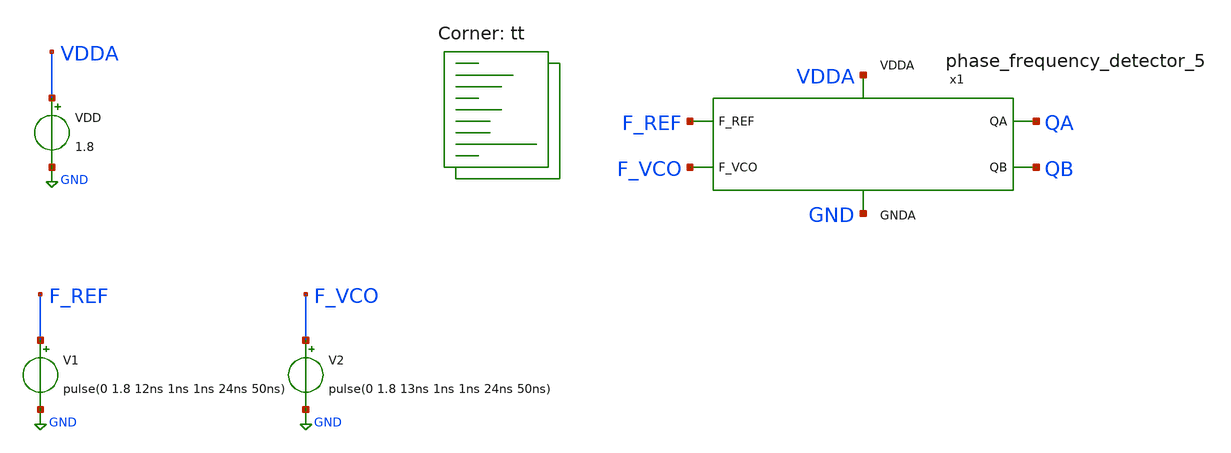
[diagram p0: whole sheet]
** sch_path: projects/pll/pfd/xschem_ngspice/tb_phase_frequency_detector.sch
**.subckt tb_phase_frequency_detector
V1 F_REF GND pulse(0 1.8 12ns 1ns 1ns 24ns 50ns)
V2 F_VCO GND pulse(0 1.8 13ns 1ns 1ns 24ns 50ns)
VDD VDDA GND 1.8
x1 F_REF F_VCO VDDA QA QB GND phase_frequency_detector_5
**** begin user architecture code
.lib $::SKYWATER_MODELS/sky130.lib.spice tt



.include /foss/pdks/sky130A/libs.ref/sky130_fd_sc_hd/spice/sky130_fd_sc_hd.spice


.option wnflag=1
.option method=gear trtol=1

* .ic v(osc)=0
* .temp = 75

.save v(x1.reset)
.save v(x1.qb_b)
.save v(x1.qa_b)
.save v(x1.f_b)
.save v(x1.f)
.save v(x1.e_b)
.save v(x1.e)
.save v(x1.before_reset)
.save v(qb)
.save v(qa)
.save v(f_vco)
.save v(f_ref)
.save v(f_vco)


.control

  tran 1ns 1us
  remzerovec
  * write tb_phase_frequency_detector.raw
  write tb_phase_frequency_detector_2.raw
  * linearize v(qa) v(qb)
  * wrdata
+ /foss/designs/my_design/projects/pll/pfd/xschem_ngspice/tb_phase_frequency_detector_QA.txt v(qa)
  * wrdata
+ /foss/designs/my_design/projects/pll/pfd/xschem_ngspice/tb_phase_frequency_detector_QB.txt v(qb)

  set appendwrite

.endc






**** end user architecture code
**.ends

* expanding   symbol:
*+  /foss/designs/my_design/projects/pll/pfd/xschem_ngspice/phase_frequency_detector_5.sym # of pins=6
** sym_path: projects/pll/pfd/xschem_ngspice/phase_frequency_detector_5.sym
** sch_path: projects/pll/pfd/xschem_ngspice/phase_frequency_detector_5.sch
.subckt phase_frequency_detector_5 F_REF F_VCO VDDA QA QB GNDA
*.ipin F_REF
*.opin QA
*.ipin F_VCO
*.opin QB
*.ipin VDDA
*.ipin GNDA
x1 VDDA GNDA QA F_REF QA_b nor_pfd
x2 VDDA GNDA QB F_VCO QB_b nor_pfd
x3 VDDA GNDA QA_b E QA nor_pfd
x4 VDDA GNDA QB_b F QB nor_pfd
x5 VDDA GNDA E_b QA_b E nor_pfd
x6 VDDA GNDA F_b QB_b F nor_pfd
x7 VDDA GNDA E Reset E_b nor_pfd
x12 VDDA GNDA F Reset F_b nor_pfd
x8 VDDA GNDA QB QA before_Reset nand_pfd
x9 VDDA GNDA before_Reset net1 inv_pfd
x10 VDDA GNDA net1 net2 inv_pfd
x11 VDDA GNDA net2 net3 inv_pfd
x13 VDDA GNDA net3 net4 inv_pfd
x14 VDDA GNDA net4 Reset inv_pfd
.ends


* expanding   symbol:  /foss/designs/my_design/projects/pll/pfd/xschem_ngspice/nor_pfd.sym # of
*+ pins=5
** sym_path: projects/pll/pfd/xschem_ngspice/nor_pfd.sym
** sch_path: projects/pll/pfd/xschem_ngspice/nor_pfd.sch
.subckt nor_pfd VDDA GNDA A B Y
*.ipin A
*.opin Y
*.ipin VDDA
*.ipin GNDA
*.ipin B
XM4 net1 B VDDA VDDA sky130_fd_pr__pfet_01v8 L=0.15 W=2 nf=1 ad='int((nf+1)/2) * W/nf * 0.29' as='int((nf+2)/2) * W/nf * 0.29'
+ pd='2*int((nf+1)/2) * (W/nf + 0.29)' ps='2*int((nf+2)/2) * (W/nf + 0.29)' nrd='0.29 / W' nrs='0.29 / W'
+ sa=0 sb=0 sd=0 mult=1 m=1
XM2 GNDA B Y GNDA sky130_fd_pr__nfet_01v8 L=0.15 W=1 nf=1 ad='int((nf+1)/2) * W/nf * 0.29' as='int((nf+2)/2) * W/nf * 0.29'
+ pd='2*int((nf+1)/2) * (W/nf + 0.29)' ps='2*int((nf+2)/2) * (W/nf + 0.29)' nrd='0.29 / W' nrs='0.29 / W'
+ sa=0 sb=0 sd=0 mult=1 m=1
XM1 GNDA A Y GNDA sky130_fd_pr__nfet_01v8 L=0.15 W=1 nf=1 ad='int((nf+1)/2) * W/nf * 0.29' as='int((nf+2)/2) * W/nf * 0.29'
+ pd='2*int((nf+1)/2) * (W/nf + 0.29)' ps='2*int((nf+2)/2) * (W/nf + 0.29)' nrd='0.29 / W' nrs='0.29 / W'
+ sa=0 sb=0 sd=0 mult=1 m=1
XM3 Y A net1 VDDA sky130_fd_pr__pfet_01v8 L=0.15 W=2 nf=1 ad='int((nf+1)/2) * W/nf * 0.29' as='int((nf+2)/2) * W/nf * 0.29'
+ pd='2*int((nf+1)/2) * (W/nf + 0.29)' ps='2*int((nf+2)/2) * (W/nf + 0.29)' nrd='0.29 / W' nrs='0.29 / W'
+ sa=0 sb=0 sd=0 mult=1 m=1
.ends


* expanding   symbol:  /foss/designs/my_design/projects/pll/pfd/xschem_ngspice/nand_pfd.sym # of
*+ pins=5
** sym_path: projects/pll/pfd/xschem_ngspice/nand_pfd.sym
** sch_path: projects/pll/pfd/xschem_ngspice/nand_pfd.sch
.subckt nand_pfd VDDA GNDA A B Y
*.ipin A
*.opin Y
*.ipin VDDA
*.ipin GNDA
*.ipin B
XM4 Y B VDDA VDDA sky130_fd_pr__pfet_01v8 L=0.15 W=1 nf=2 ad='int((nf+1)/2) * W/nf * 0.29' as='int((nf+2)/2) * W/nf * 0.29'
+ pd='2*int((nf+1)/2) * (W/nf + 0.29)' ps='2*int((nf+2)/2) * (W/nf + 0.29)' nrd='0.29 / W' nrs='0.29 / W'
+ sa=0 sb=0 sd=0 mult=1 m=1
XM2 net1 B Y GNDA sky130_fd_pr__nfet_01v8 L=0.15 W=0.5 nf=1 ad='int((nf+1)/2) * W/nf * 0.29' as='int((nf+2)/2) * W/nf * 0.29'
+ pd='2*int((nf+1)/2) * (W/nf + 0.29)' ps='2*int((nf+2)/2) * (W/nf + 0.29)' nrd='0.29 / W' nrs='0.29 / W'
+ sa=0 sb=0 sd=0 mult=1 m=1
XM1 GNDA A net1 GNDA sky130_fd_pr__nfet_01v8 L=0.15 W=0.5 nf=1 ad='int((nf+1)/2) * W/nf * 0.29' as='int((nf+2)/2) * W/nf * 0.29'
+ pd='2*int((nf+1)/2) * (W/nf + 0.29)' ps='2*int((nf+2)/2) * (W/nf + 0.29)' nrd='0.29 / W' nrs='0.29 / W'
+ sa=0 sb=0 sd=0 mult=1 m=1
XM3 Y A VDDA VDDA sky130_fd_pr__pfet_01v8 L=0.15 W=1 nf=2 ad='int((nf+1)/2) * W/nf * 0.29' as='int((nf+2)/2) * W/nf * 0.29'
+ pd='2*int((nf+1)/2) * (W/nf + 0.29)' ps='2*int((nf+2)/2) * (W/nf + 0.29)' nrd='0.29 / W' nrs='0.29 / W'
+ sa=0 sb=0 sd=0 mult=1 m=1
.ends


* expanding   symbol:  /foss/designs/my_design/projects/pll/pfd/xschem_ngspice/inv_pfd.sym # of
*+ pins=4
** sym_path: projects/ASU/EEE572/schematic/inv_pfd.sym
** sch_path: projects/ASU/EEE572/schematic/inv_pfd.sch
.subckt inv_pfd VDDA GNDA A Y
*.ipin A
*.opin Y
*.ipin VDDA
*.ipin GNDA
XM2 Y A VDDA VDDA sky130_fd_pr__pfet_01v8 L=0.15 W=2 nf=1 ad='int((nf+1)/2) * W/nf * 0.29' as='int((nf+2)/2) * W/nf * 0.29'
+ pd='2*int((nf+1)/2) * (W/nf + 0.29)' ps='2*int((nf+2)/2) * (W/nf + 0.29)' nrd='0.29 / W' nrs='0.29 / W'
+ sa=0 sb=0 sd=0 mult=1 m=1
XM1 GNDA A Y GNDA sky130_fd_pr__nfet_01v8 L=0.15 W=1 nf=1 ad='int((nf+1)/2) * W/nf * 0.29' as='int((nf+2)/2) * W/nf * 0.29'
+ pd='2*int((nf+1)/2) * (W/nf + 0.29)' ps='2*int((nf+2)/2) * (W/nf + 0.29)' nrd='0.29 / W' nrs='0.29 / W'
+ sa=0 sb=0 sd=0 mult=1 m=1
.ends

.GLOBAL GND
.end
